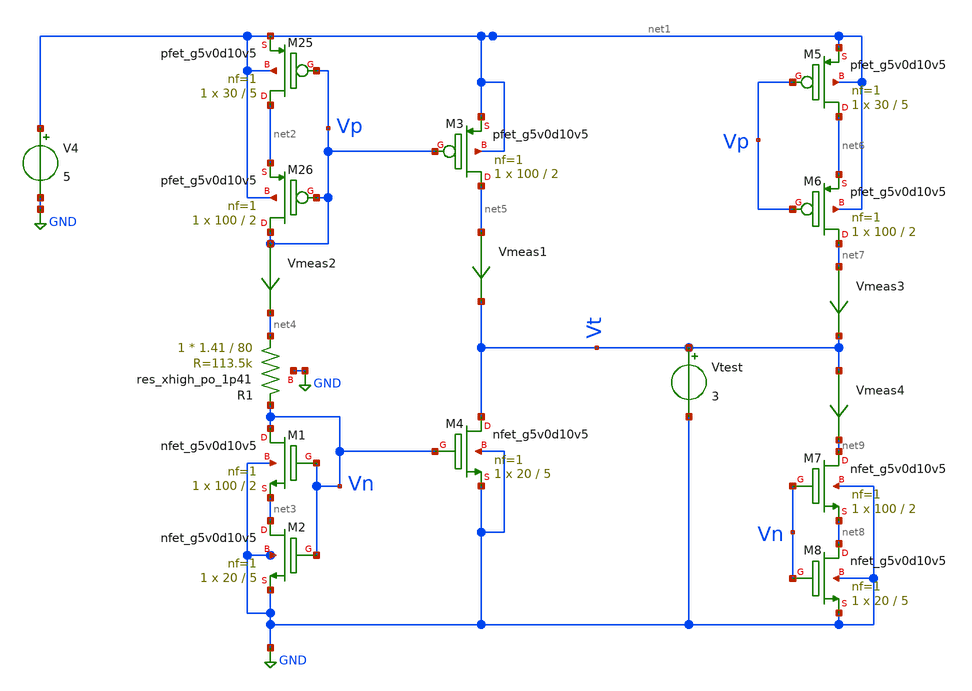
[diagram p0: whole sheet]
** sch_path: xschem/PrimalStructures/CurRef0.sch
**.subckt CurRef0
XM25 net2 Vp net1 net1 sky130_fd_pr__pfet_g5v0d10v5 L=5 W=30 nf=1 ad='int((nf+1)/2) * W/nf * 0.29' as='int((nf+2)/2) * W/nf * 0.29'
+ pd='2*int((nf+1)/2) * (W/nf + 0.29)' ps='2*int((nf+2)/2) * (W/nf + 0.29)' nrd='0.29 / W' nrs='0.29 / W'
+ sa=0 sb=0 sd=0 mult=1 m=1
XM26 Vp Vp net2 net1 sky130_fd_pr__pfet_g5v0d10v5 L=2 W=100 nf=1 ad='int((nf+1)/2) * W/nf * 0.29' as='int((nf+2)/2) * W/nf * 0.29'
+ pd='2*int((nf+1)/2) * (W/nf + 0.29)' ps='2*int((nf+2)/2) * (W/nf + 0.29)' nrd='0.29 / W' nrs='0.29 / W'
+ sa=0 sb=0 sd=0 mult=1 m=1
V4 net1 GND 5
XR1 net4 Vn GND sky130_fd_pr__res_xhigh_po_1p41 L=80 mult=1 m=1
Vmeas2 Vp net4 0
.save i(vmeas2)
XM1 Vn Vn net3 GND sky130_fd_pr__nfet_g5v0d10v5 L=2 W=100 nf=1 ad='int((nf+1)/2) * W/nf * 0.29' as='int((nf+2)/2) * W/nf * 0.29'
+ pd='2*int((nf+1)/2) * (W/nf + 0.29)' ps='2*int((nf+2)/2) * (W/nf + 0.29)' nrd='0.29 / W' nrs='0.29 / W'
+ sa=0 sb=0 sd=0 mult=1 m=1
XM2 net3 Vn GND GND sky130_fd_pr__nfet_g5v0d10v5 L=5 W=20 nf=1 ad='int((nf+1)/2) * W/nf * 0.29' as='int((nf+2)/2) * W/nf * 0.29'
+ pd='2*int((nf+1)/2) * (W/nf + 0.29)' ps='2*int((nf+2)/2) * (W/nf + 0.29)' nrd='0.29 / W' nrs='0.29 / W'
+ sa=0 sb=0 sd=0 mult=1 m=1
XM3 net5 Vp net1 net1 sky130_fd_pr__pfet_g5v0d10v5 L=2 W=100 nf=1 ad='int((nf+1)/2) * W/nf * 0.29' as='int((nf+2)/2) * W/nf * 0.29'
+ pd='2*int((nf+1)/2) * (W/nf + 0.29)' ps='2*int((nf+2)/2) * (W/nf + 0.29)' nrd='0.29 / W' nrs='0.29 / W'
+ sa=0 sb=0 sd=0 mult=1 m=1
Vmeas1 net5 Vt 0
.save i(vmeas1)
XM4 Vt Vn GND GND sky130_fd_pr__nfet_g5v0d10v5 L=5 W=20 nf=1 ad='int((nf+1)/2) * W/nf * 0.29' as='int((nf+2)/2) * W/nf * 0.29'
+ pd='2*int((nf+1)/2) * (W/nf + 0.29)' ps='2*int((nf+2)/2) * (W/nf + 0.29)' nrd='0.29 / W' nrs='0.29 / W'
+ sa=0 sb=0 sd=0 mult=1 m=1
Vtest Vt GND 3
XM5 net6 Vp net1 net1 sky130_fd_pr__pfet_g5v0d10v5 L=5 W=30 nf=1 ad='int((nf+1)/2) * W/nf * 0.29' as='int((nf+2)/2) * W/nf * 0.29'
+ pd='2*int((nf+1)/2) * (W/nf + 0.29)' ps='2*int((nf+2)/2) * (W/nf + 0.29)' nrd='0.29 / W' nrs='0.29 / W'
+ sa=0 sb=0 sd=0 mult=1 m=1
XM6 net7 Vp net6 net1 sky130_fd_pr__pfet_g5v0d10v5 L=2 W=100 nf=1 ad='int((nf+1)/2) * W/nf * 0.29' as='int((nf+2)/2) * W/nf * 0.29'
+ pd='2*int((nf+1)/2) * (W/nf + 0.29)' ps='2*int((nf+2)/2) * (W/nf + 0.29)' nrd='0.29 / W' nrs='0.29 / W'
+ sa=0 sb=0 sd=0 mult=1 m=1
Vmeas3 net7 Vt 0
.save i(vmeas3)
Vmeas4 Vt net9 0
.save i(vmeas4)
XM7 net9 Vn net8 GND sky130_fd_pr__nfet_g5v0d10v5 L=2 W=100 nf=1 ad='int((nf+1)/2) * W/nf * 0.29' as='int((nf+2)/2) * W/nf * 0.29'
+ pd='2*int((nf+1)/2) * (W/nf + 0.29)' ps='2*int((nf+2)/2) * (W/nf + 0.29)' nrd='0.29 / W' nrs='0.29 / W'
+ sa=0 sb=0 sd=0 mult=1 m=1
XM8 net8 Vn GND GND sky130_fd_pr__nfet_g5v0d10v5 L=5 W=20 nf=1 ad='int((nf+1)/2) * W/nf * 0.29' as='int((nf+2)/2) * W/nf * 0.29'
+ pd='2*int((nf+1)/2) * (W/nf + 0.29)' ps='2*int((nf+2)/2) * (W/nf + 0.29)' nrd='0.29 / W' nrs='0.29 / W'
+ sa=0 sb=0 sd=0 mult=1 m=1
**** begin user architecture code

** opencircuitdesign pdks install
.lib $::SKYWATER_MODELS/sky130.lib.spice tt




.control
op
print all
save all
dc Vtest 1 4 0.01
plot I(Vmeas3), I(Vmeas4) vs V(Vt)
.endc


**** end user architecture code
**.ends
.GLOBAL GND
.end
